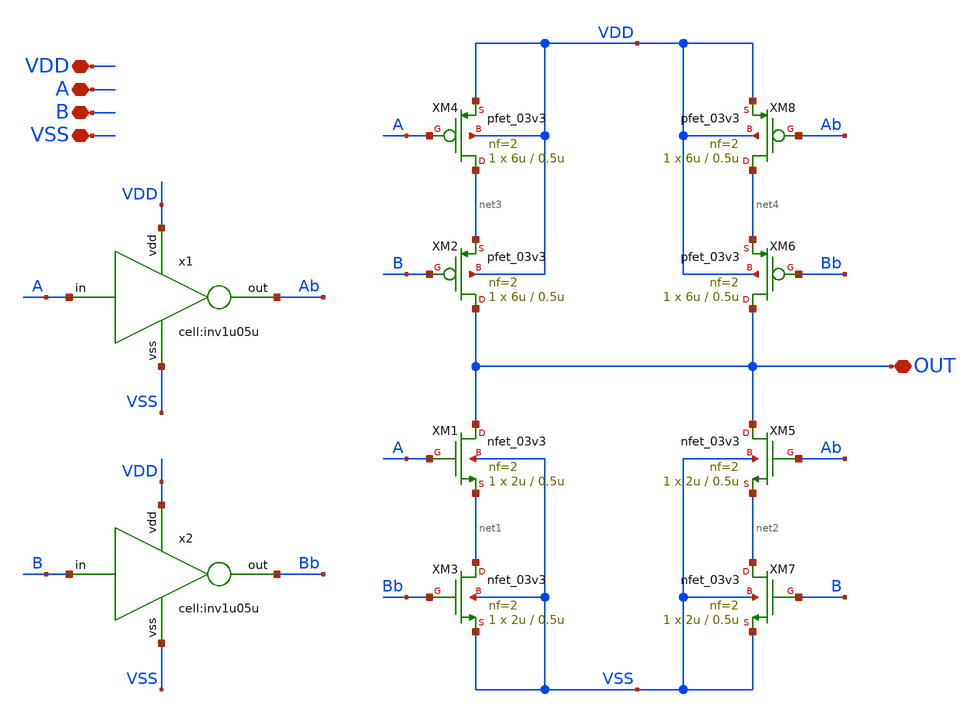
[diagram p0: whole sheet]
** sch_path: designs/libs/core_analog/asc_XNOR/asc_XNOR.sch
**.subckt asc_XNOR VDD VSS B A OUT
*.iopin VDD
*.iopin VSS
*.iopin B
*.iopin A
*.iopin OUT
XM1 OUT A net1 VSS nfet_03v3 L=0.5u W=2u nf=2 ad='int((nf+1)/2) * W/nf * 0.18u' as='int((nf+2)/2) * W/nf * 0.18u'
+ pd='2*int((nf+1)/2) * (W/nf + 0.18u)' ps='2*int((nf+2)/2) * (W/nf + 0.18u)' nrd='0.18u / W' nrs='0.18u / W'
+ sa=0 sb=0 sd=0 m=1
XM2 OUT B net3 VDD pfet_03v3 L=0.5u W=6u nf=2 ad='int((nf+1)/2) * W/nf * 0.18u' as='int((nf+2)/2) * W/nf * 0.18u'
+ pd='2*int((nf+1)/2) * (W/nf + 0.18u)' ps='2*int((nf+2)/2) * (W/nf + 0.18u)' nrd='0.18u / W' nrs='0.18u / W'
+ sa=0 sb=0 sd=0 m=1
XM3 net1 Bb VSS VSS nfet_03v3 L=0.5u W=2u nf=2 ad='int((nf+1)/2) * W/nf * 0.18u' as='int((nf+2)/2) * W/nf * 0.18u'
+ pd='2*int((nf+1)/2) * (W/nf + 0.18u)' ps='2*int((nf+2)/2) * (W/nf + 0.18u)' nrd='0.18u / W' nrs='0.18u / W'
+ sa=0 sb=0 sd=0 m=1
XM4 net3 A VDD VDD pfet_03v3 L=0.5u W=6u nf=2 ad='int((nf+1)/2) * W/nf * 0.18u' as='int((nf+2)/2) * W/nf * 0.18u'
+ pd='2*int((nf+1)/2) * (W/nf + 0.18u)' ps='2*int((nf+2)/2) * (W/nf + 0.18u)' nrd='0.18u / W' nrs='0.18u / W'
+ sa=0 sb=0 sd=0 m=1
XM5 OUT Ab net2 VSS nfet_03v3 L=0.5u W=2u nf=2 ad='int((nf+1)/2) * W/nf * 0.18u' as='int((nf+2)/2) * W/nf * 0.18u'
+ pd='2*int((nf+1)/2) * (W/nf + 0.18u)' ps='2*int((nf+2)/2) * (W/nf + 0.18u)' nrd='0.18u / W' nrs='0.18u / W'
+ sa=0 sb=0 sd=0 m=1
XM6 OUT Bb net4 VDD pfet_03v3 L=0.5u W=6u nf=2 ad='int((nf+1)/2) * W/nf * 0.18u' as='int((nf+2)/2) * W/nf * 0.18u'
+ pd='2*int((nf+1)/2) * (W/nf + 0.18u)' ps='2*int((nf+2)/2) * (W/nf + 0.18u)' nrd='0.18u / W' nrs='0.18u / W'
+ sa=0 sb=0 sd=0 m=1
XM7 net2 B VSS VSS nfet_03v3 L=0.5u W=2u nf=2 ad='int((nf+1)/2) * W/nf * 0.18u' as='int((nf+2)/2) * W/nf * 0.18u'
+ pd='2*int((nf+1)/2) * (W/nf + 0.18u)' ps='2*int((nf+2)/2) * (W/nf + 0.18u)' nrd='0.18u / W' nrs='0.18u / W'
+ sa=0 sb=0 sd=0 m=1
XM8 net4 Ab VDD VDD pfet_03v3 L=0.5u W=6u nf=2 ad='int((nf+1)/2) * W/nf * 0.18u' as='int((nf+2)/2) * W/nf * 0.18u'
+ pd='2*int((nf+1)/2) * (W/nf + 0.18u)' ps='2*int((nf+2)/2) * (W/nf + 0.18u)' nrd='0.18u / W' nrs='0.18u / W'
+ sa=0 sb=0 sd=0 m=1
x1 A VDD Ab VSS inv1u05u
x2 B VDD Bb VSS inv1u05u
**.ends
.end
